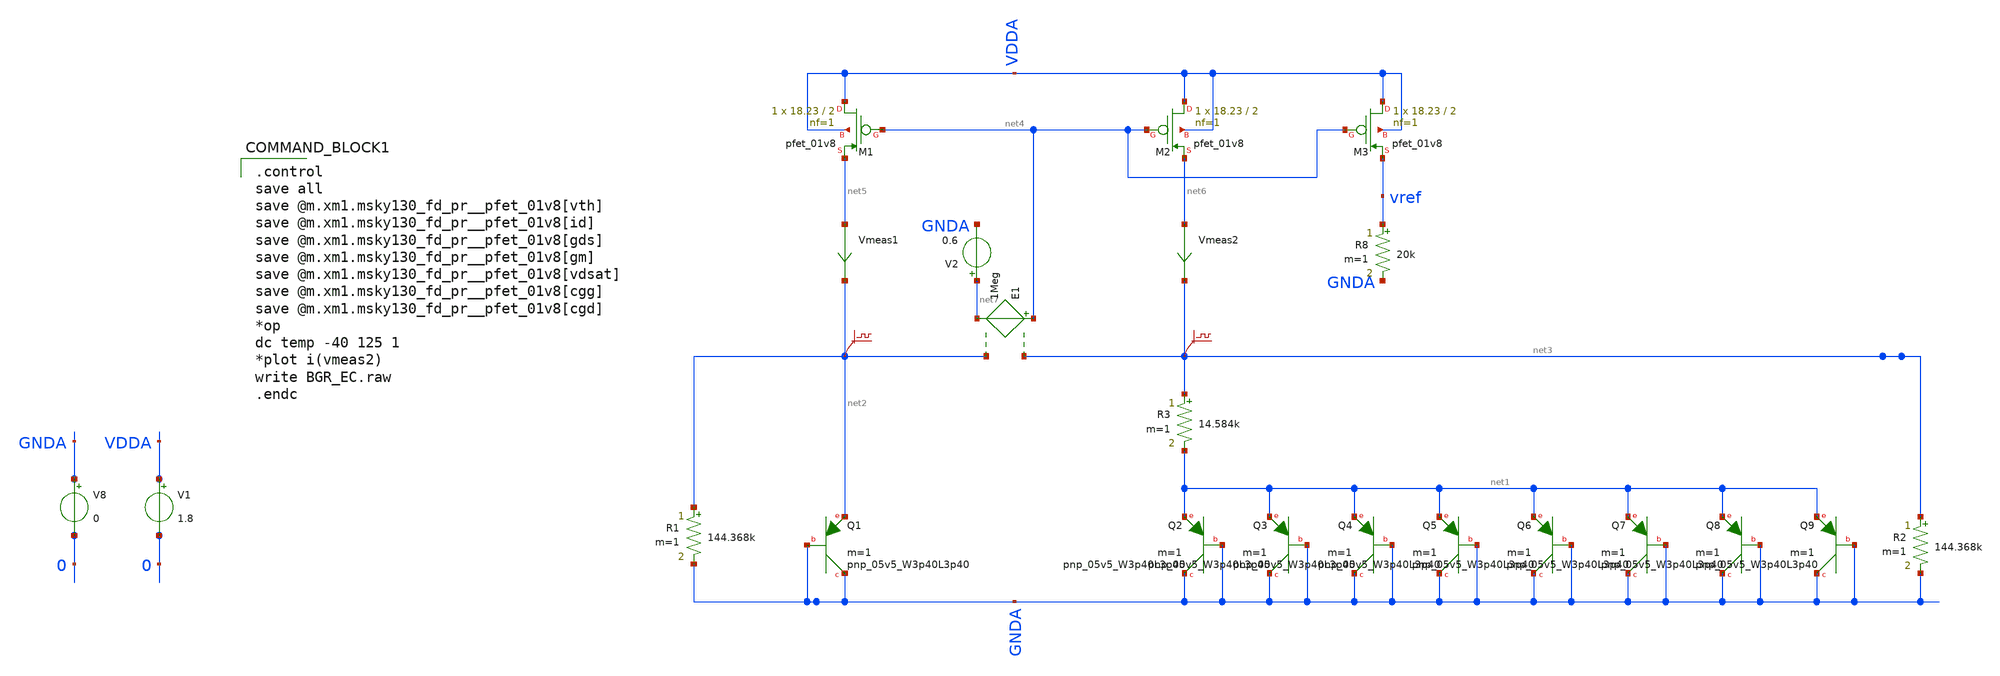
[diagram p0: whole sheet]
** sch_path: BGR_EC.sch
**.subckt BGR_EC
XQ1 GNDA GNDA net2 sky130_fd_pr__pnp_05v5_W3p40L3p40 m=1
XQ2 GNDA GNDA net1 sky130_fd_pr__pnp_05v5_W3p40L3p40 m=1
XQ3 GNDA GNDA net1 sky130_fd_pr__pnp_05v5_W3p40L3p40 m=1
XQ4 GNDA GNDA net1 sky130_fd_pr__pnp_05v5_W3p40L3p40 m=1
XQ5 GNDA GNDA net1 sky130_fd_pr__pnp_05v5_W3p40L3p40 m=1
XQ6 GNDA GNDA net1 sky130_fd_pr__pnp_05v5_W3p40L3p40 m=1
XQ7 GNDA GNDA net1 sky130_fd_pr__pnp_05v5_W3p40L3p40 m=1
XQ8 GNDA GNDA net1 sky130_fd_pr__pnp_05v5_W3p40L3p40 m=1
XQ9 GNDA GNDA net1 sky130_fd_pr__pnp_05v5_W3p40L3p40 m=1
V8 GNDA 0 0
.save v(net2)
.save v(net3)
XM1 VDDA net4 net5 VDDA sky130_fd_pr__pfet_01v8 L=2 W=18.23 nf=1 ad='int((nf+1)/2) * W/nf * 0.29' as='int((nf+2)/2) * W/nf * 0.29'
+ pd='2*int((nf+1)/2) * (W/nf + 0.29)' ps='2*int((nf+2)/2) * (W/nf + 0.29)' nrd='0.29 / W' nrs='0.29 / W'
+ sa=0 sb=0 sd=0 mult=1 m=1
XM2 VDDA net4 net6 VDDA sky130_fd_pr__pfet_01v8 L=2 W=18.23 nf=1 ad='int((nf+1)/2) * W/nf * 0.29' as='int((nf+2)/2) * W/nf * 0.29'
+ pd='2*int((nf+1)/2) * (W/nf + 0.29)' ps='2*int((nf+2)/2) * (W/nf + 0.29)' nrd='0.29 / W' nrs='0.29 / W'
+ sa=0 sb=0 sd=0 mult=1 m=1
V1 VDDA 0 1.8
E1 net4 net7 net3 net2 1Meg
V2 net7 GNDA 0.6
Vmeas1 net5 net2 0
.save i(vmeas1)
Vmeas2 net6 net3 0
.save i(vmeas2)
R8 vref GNDA 20k m=1
XM3 VDDA net4 vref VDDA sky130_fd_pr__pfet_01v8 L=2 W=18.23 nf=1 ad='int((nf+1)/2) * W/nf * 0.29' as='int((nf+2)/2) * W/nf * 0.29'
+ pd='2*int((nf+1)/2) * (W/nf + 0.29)' ps='2*int((nf+2)/2) * (W/nf + 0.29)' nrd='0.29 / W' nrs='0.29 / W'
+ sa=0 sb=0 sd=0 mult=1 m=1
R1 net2 GNDA 144.368k m=1
R3 net3 net1 14.584k m=1
R2 net3 GNDA 144.368k m=1
**** begin user architecture code

** opencircuitdesign pdks install
.lib $::SKYWATER_MODELS/sky130.lib.spice tt



.control
save all
save @m.xm1.msky130_fd_pr__pfet_01v8[vth]
save @m.xm1.msky130_fd_pr__pfet_01v8[id]
save @m.xm1.msky130_fd_pr__pfet_01v8[gds]
save @m.xm1.msky130_fd_pr__pfet_01v8[gm]
save @m.xm1.msky130_fd_pr__pfet_01v8[vdsat]
save @m.xm1.msky130_fd_pr__pfet_01v8[cgg]
save @m.xm1.msky130_fd_pr__pfet_01v8[cgd]
*op
dc temp -40 125 1
*plot i(vmeas2)
write BGR_EC.raw
.endc

**** end user architecture code
**.ends
.end
